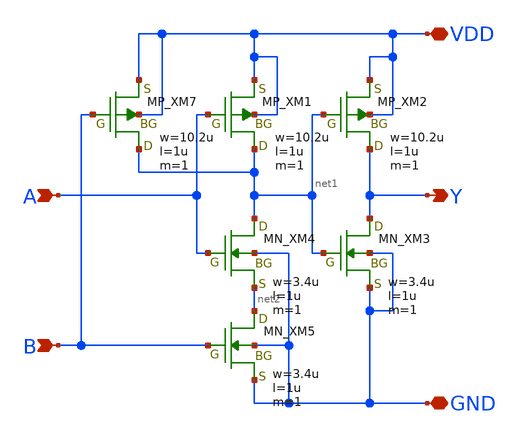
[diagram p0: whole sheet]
** sch_path: openIP62_rev1.0/IP62/Technology/tech/symbols/Xschem/IP62_5_stdcell/AND2_X1.sch
**.subckt AND2_X1 Y A B VDD GND
*.opin Y
*.ipin A
*.ipin B
*.iopin VDD
*.iopin GND
XM7 net1 B VDD VDD PMOS w=10.2u l=1u as=0 ad=0 ps=0 pd=0 nrd=0 nrs=0 m=1
XM1 net1 A VDD VDD PMOS w=10.2u l=1u as=0 ad=0 ps=0 pd=0 nrd=0 nrs=0 m=1
XM2 Y net1 VDD VDD PMOS w=10.2u l=1u as=0 ad=0 ps=0 pd=0 nrd=0 nrs=0 m=1
XM3 Y net1 GND GND NMOS w=3.4u l=1u as=0 ad=0 ps=0 pd=0 nrd=0 nrs=0 m=1
XM4 net1 A net2 GND NMOS w=3.4u l=1u as=0 ad=0 ps=0 pd=0 nrd=0 nrs=0 m=1
XM5 net2 B GND GND NMOS w=3.4u l=1u as=0 ad=0 ps=0 pd=0 nrd=0 nrs=0 m=1
**.ends
.end
